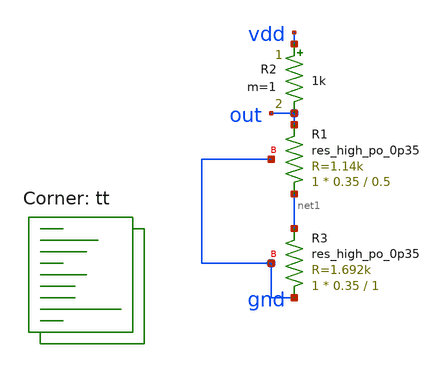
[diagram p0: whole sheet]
** sch_path: xschem/res_seg_1-tb.sch
**.subckt res_seg_1-tb
XR1 net1 out gnd sky130_fd_pr__res_high_po_0p35 L=0.5 mult=1 m=1
R2 vdd out 1k m=1
XR3 gnd net1 gnd sky130_fd_pr__res_high_po_0p35 L=1 mult=1 m=1
**** begin user architecture code



  .param max_freq=500e3 period={1/max_freq} time_high={period/2}
  .param delay_vin1={time_high} delay_vin2={time_high*1.5}
  .param lval=100u

  .option wnflag=1
  .option safecurrents

  Vddh vdd gnd dc 5
  *Vin  in  gnd pulse(0 1.8 {delay_vin1} 1p 1p {time_high} {period})
  *Vinb inb gnd pulse(1.8 0 {delay_vin1} 1p 1p {time_high} {period})

  .control
     reset
     save all
     dc vddh 0 5 0.001
     write res_segment.raw
     set appendwrite

     *reset
     *save all
     *dc vref 0 1.8 0.1
     *write lvsf-tb.raw
*    quit 0
  .endc



.lib $::SKYWATER_MODELS/sky130.lib.spice tt
**** end user architecture code
**.ends
.end
